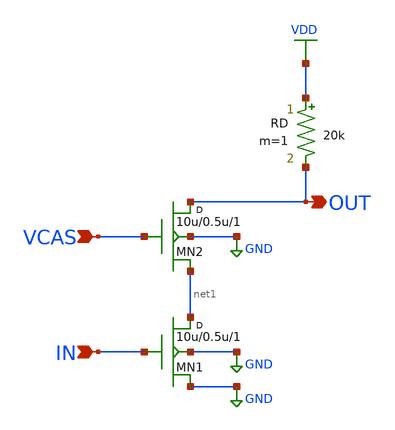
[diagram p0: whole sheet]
** sch_path: E3_238_Analog_VLSI_Circuits/10_Cascode_Amplifier/cs_cascode.sch
**.subckt cs_cascode IN VCAS OUT
*.ipin IN
*.ipin VCAS
*.opin OUT
MN1 net1 IN GND GND nmos w=10u l=0.5u m=1
MN2 OUT VCAS net1 GND nmos w=10u l=0.5u m=1
RD VDD OUT 20k m=1
**** begin user architecture code

.include /home/anirudh/Analog_VLSI_Projects/models/cmos_180nm.mod
VDD VDD 0 DC 1.8
VIN IN 0 DC 0.57 AC 1
VCAS VCAS 0 DC 1.0
CL OUT GND 1p

.control
  op
  print v(OUT)
  ac dec 20 1 1G
  plot db(v(OUT))
  plot phase(v(OUT))*180/pi
.endc


**** end user architecture code
**.ends
.GLOBAL VDD
.GLOBAL GND
.end
